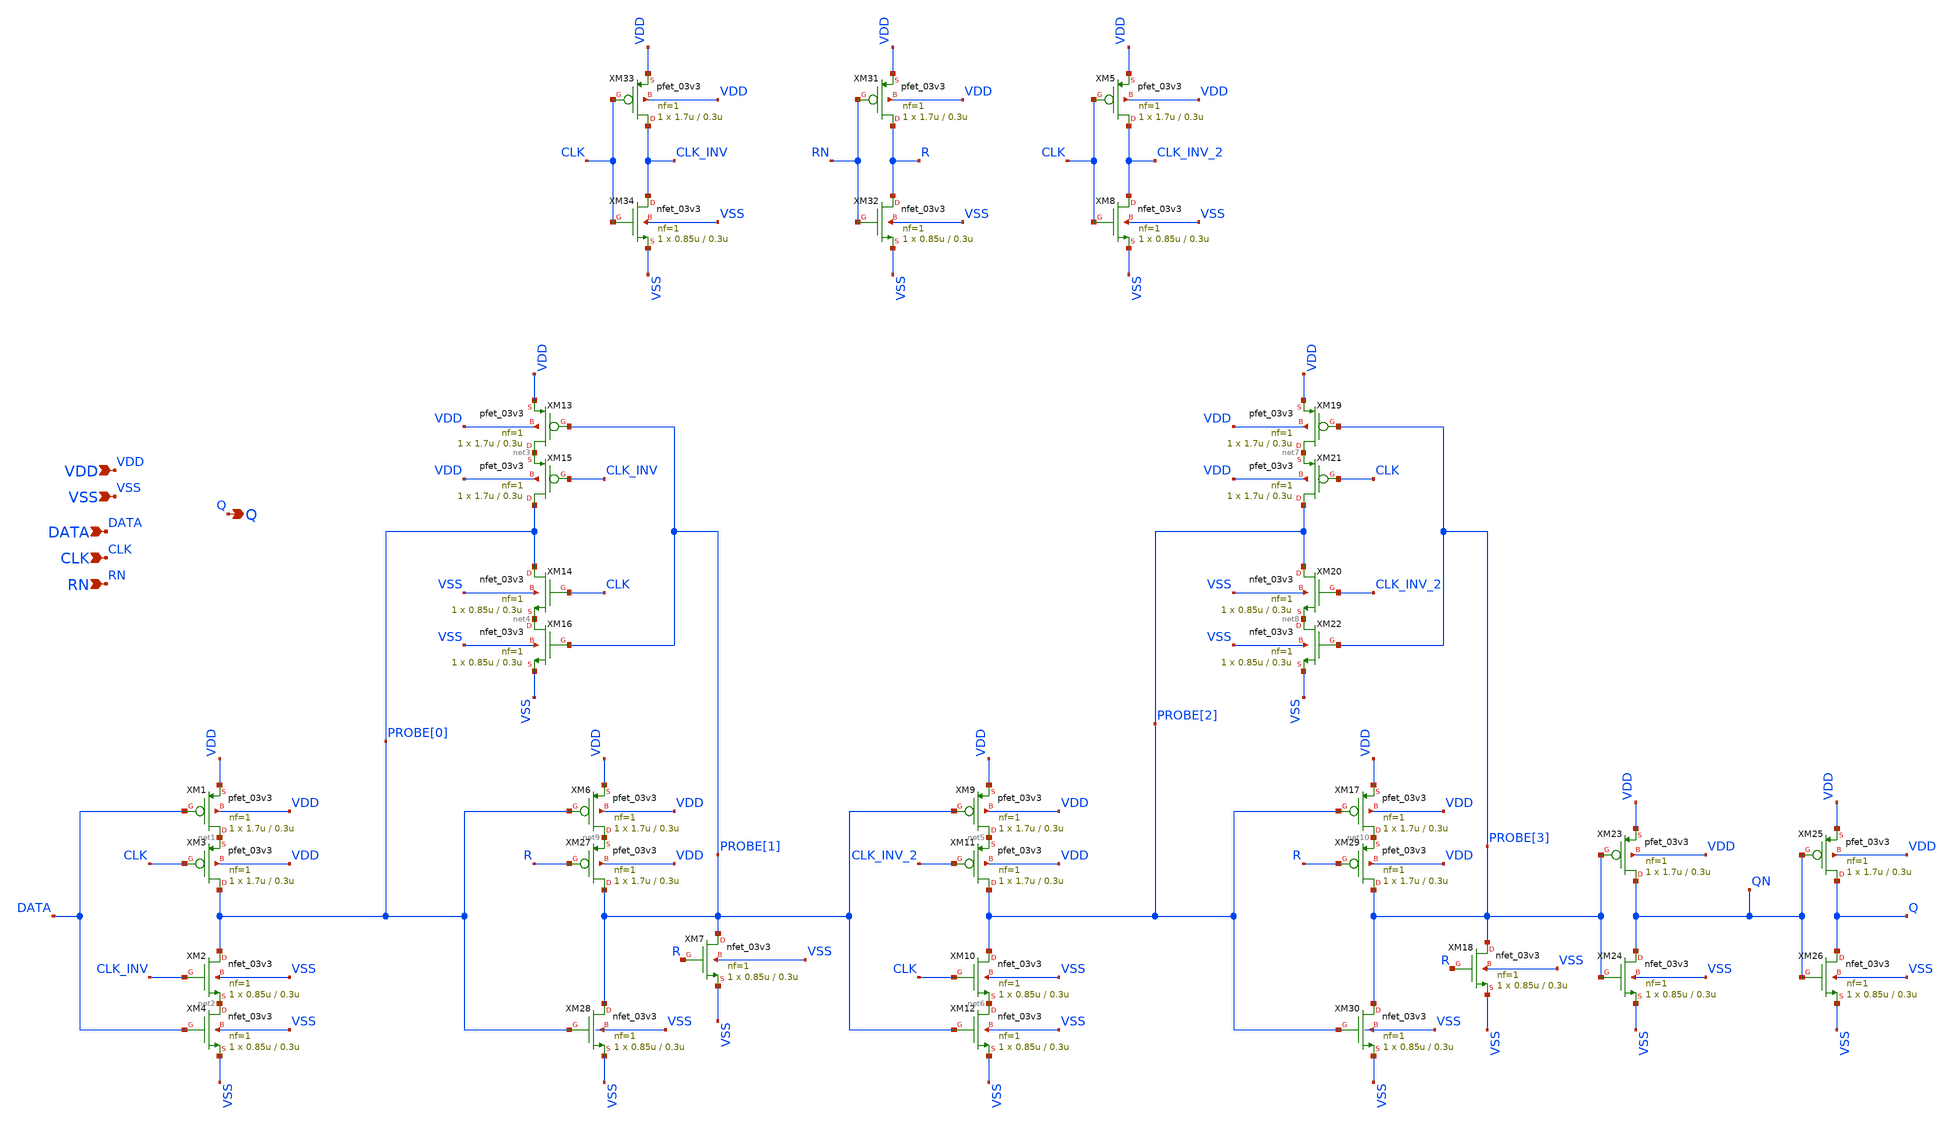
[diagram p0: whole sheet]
** sch_path: designs/cells/gf180mcu_voidwalkers_sc_sdffrnq_4/sch/d_flip_flop_r.sch
**.subckt d_flip_flop_r DATA VDD VSS Q CLK RN
*.ipin DATA
*.ipin VDD
*.ipin VSS
*.opin Q
*.ipin CLK
*.ipin RN
XM1 net1 DATA VDD VDD pfet_03v3 L=0.3u W=1.7u nf=1 ad='int((nf+1)/2) * W/nf * 0.18u' as='int((nf+2)/2) * W/nf * 0.18u'
+ pd='2*int((nf+1)/2) * (W/nf + 0.18u)' ps='2*int((nf+2)/2) * (W/nf + 0.18u)' nrd='0.18u / W' nrs='0.18u / W'
+ sa=0 sb=0 sd=0 m=1
XM2 PROBE[0] CLK_INV net2 VSS nfet_03v3 L=0.3u W=0.85u nf=1 ad='int((nf+1)/2) * W/nf * 0.18u' as='int((nf+2)/2) * W/nf * 0.18u'
+ pd='2*int((nf+1)/2) * (W/nf + 0.18u)' ps='2*int((nf+2)/2) * (W/nf + 0.18u)' nrd='0.18u / W' nrs='0.18u / W'
+ sa=0 sb=0 sd=0 m=1
XM3 PROBE[0] CLK net1 VDD pfet_03v3 L=0.3u W=1.7u nf=1 ad='int((nf+1)/2) * W/nf * 0.18u' as='int((nf+2)/2) * W/nf * 0.18u'
+ pd='2*int((nf+1)/2) * (W/nf + 0.18u)' ps='2*int((nf+2)/2) * (W/nf + 0.18u)' nrd='0.18u / W' nrs='0.18u / W'
+ sa=0 sb=0 sd=0 m=1
XM4 net2 DATA VSS VSS nfet_03v3 L=0.3u W=0.85u nf=1 ad='int((nf+1)/2) * W/nf * 0.18u' as='int((nf+2)/2) * W/nf * 0.18u'
+ pd='2*int((nf+1)/2) * (W/nf + 0.18u)' ps='2*int((nf+2)/2) * (W/nf + 0.18u)' nrd='0.18u / W' nrs='0.18u / W'
+ sa=0 sb=0 sd=0 m=1
XM5 CLK_INV_2 CLK VDD VDD pfet_03v3 L=0.3u W=1.7u nf=1 ad='int((nf+1)/2) * W/nf * 0.18u' as='int((nf+2)/2) * W/nf * 0.18u'
+ pd='2*int((nf+1)/2) * (W/nf + 0.18u)' ps='2*int((nf+2)/2) * (W/nf + 0.18u)' nrd='0.18u / W' nrs='0.18u / W'
+ sa=0 sb=0 sd=0 m=1
XM8 CLK_INV_2 CLK VSS VSS nfet_03v3 L=0.3u W=0.85u nf=1 ad='int((nf+1)/2) * W/nf * 0.18u' as='int((nf+2)/2) * W/nf * 0.18u'
+ pd='2*int((nf+1)/2) * (W/nf + 0.18u)' ps='2*int((nf+2)/2) * (W/nf + 0.18u)' nrd='0.18u / W' nrs='0.18u / W'
+ sa=0 sb=0 sd=0 m=1
XM13 net3 PROBE[1] VDD VDD pfet_03v3 L=0.3u W=1.7u nf=1 ad='int((nf+1)/2) * W/nf * 0.18u' as='int((nf+2)/2) * W/nf * 0.18u'
+ pd='2*int((nf+1)/2) * (W/nf + 0.18u)' ps='2*int((nf+2)/2) * (W/nf + 0.18u)' nrd='0.18u / W' nrs='0.18u / W'
+ sa=0 sb=0 sd=0 m=1
XM14 PROBE[0] CLK net4 VSS nfet_03v3 L=0.3u W=0.85u nf=1 ad='int((nf+1)/2) * W/nf * 0.18u' as='int((nf+2)/2) * W/nf * 0.18u'
+ pd='2*int((nf+1)/2) * (W/nf + 0.18u)' ps='2*int((nf+2)/2) * (W/nf + 0.18u)' nrd='0.18u / W' nrs='0.18u / W'
+ sa=0 sb=0 sd=0 m=1
XM15 PROBE[0] CLK_INV net3 VDD pfet_03v3 L=0.3u W=1.7u nf=1 ad='int((nf+1)/2) * W/nf * 0.18u' as='int((nf+2)/2) * W/nf * 0.18u'
+ pd='2*int((nf+1)/2) * (W/nf + 0.18u)' ps='2*int((nf+2)/2) * (W/nf + 0.18u)' nrd='0.18u / W' nrs='0.18u / W'
+ sa=0 sb=0 sd=0 m=1
XM16 net4 PROBE[1] VSS VSS nfet_03v3 L=0.3u W=0.85u nf=1 ad='int((nf+1)/2) * W/nf * 0.18u' as='int((nf+2)/2) * W/nf * 0.18u'
+ pd='2*int((nf+1)/2) * (W/nf + 0.18u)' ps='2*int((nf+2)/2) * (W/nf + 0.18u)' nrd='0.18u / W' nrs='0.18u / W'
+ sa=0 sb=0 sd=0 m=1
XM9 net5 PROBE[1] VDD VDD pfet_03v3 L=0.3u W=1.7u nf=1 ad='int((nf+1)/2) * W/nf * 0.18u' as='int((nf+2)/2) * W/nf * 0.18u'
+ pd='2*int((nf+1)/2) * (W/nf + 0.18u)' ps='2*int((nf+2)/2) * (W/nf + 0.18u)' nrd='0.18u / W' nrs='0.18u / W'
+ sa=0 sb=0 sd=0 m=1
XM10 PROBE[2] CLK net6 VSS nfet_03v3 L=0.3u W=0.85u nf=1 ad='int((nf+1)/2) * W/nf * 0.18u' as='int((nf+2)/2) * W/nf * 0.18u'
+ pd='2*int((nf+1)/2) * (W/nf + 0.18u)' ps='2*int((nf+2)/2) * (W/nf + 0.18u)' nrd='0.18u / W' nrs='0.18u / W'
+ sa=0 sb=0 sd=0 m=1
XM11 PROBE[2] CLK_INV_2 net5 VDD pfet_03v3 L=0.3u W=1.7u nf=1 ad='int((nf+1)/2) * W/nf * 0.18u' as='int((nf+2)/2) * W/nf * 0.18u'
+ pd='2*int((nf+1)/2) * (W/nf + 0.18u)' ps='2*int((nf+2)/2) * (W/nf + 0.18u)' nrd='0.18u / W' nrs='0.18u / W'
+ sa=0 sb=0 sd=0 m=1
XM12 net6 PROBE[1] VSS VSS nfet_03v3 L=0.3u W=0.85u nf=1 ad='int((nf+1)/2) * W/nf * 0.18u' as='int((nf+2)/2) * W/nf * 0.18u'
+ pd='2*int((nf+1)/2) * (W/nf + 0.18u)' ps='2*int((nf+2)/2) * (W/nf + 0.18u)' nrd='0.18u / W' nrs='0.18u / W'
+ sa=0 sb=0 sd=0 m=1
XM19 net7 PROBE[3] VDD VDD pfet_03v3 L=0.3u W=1.7u nf=1 ad='int((nf+1)/2) * W/nf * 0.18u' as='int((nf+2)/2) * W/nf * 0.18u'
+ pd='2*int((nf+1)/2) * (W/nf + 0.18u)' ps='2*int((nf+2)/2) * (W/nf + 0.18u)' nrd='0.18u / W' nrs='0.18u / W'
+ sa=0 sb=0 sd=0 m=1
XM20 PROBE[2] CLK_INV_2 net8 VSS nfet_03v3 L=0.3u W=0.85u nf=1 ad='int((nf+1)/2) * W/nf * 0.18u' as='int((nf+2)/2) * W/nf * 0.18u'
+ pd='2*int((nf+1)/2) * (W/nf + 0.18u)' ps='2*int((nf+2)/2) * (W/nf + 0.18u)' nrd='0.18u / W' nrs='0.18u / W'
+ sa=0 sb=0 sd=0 m=1
XM21 PROBE[2] CLK net7 VDD pfet_03v3 L=0.3u W=1.7u nf=1 ad='int((nf+1)/2) * W/nf * 0.18u' as='int((nf+2)/2) * W/nf * 0.18u'
+ pd='2*int((nf+1)/2) * (W/nf + 0.18u)' ps='2*int((nf+2)/2) * (W/nf + 0.18u)' nrd='0.18u / W' nrs='0.18u / W'
+ sa=0 sb=0 sd=0 m=1
XM22 net8 PROBE[3] VSS VSS nfet_03v3 L=0.3u W=0.85u nf=1 ad='int((nf+1)/2) * W/nf * 0.18u' as='int((nf+2)/2) * W/nf * 0.18u'
+ pd='2*int((nf+1)/2) * (W/nf + 0.18u)' ps='2*int((nf+2)/2) * (W/nf + 0.18u)' nrd='0.18u / W' nrs='0.18u / W'
+ sa=0 sb=0 sd=0 m=1
XM23 QN PROBE[3] VDD VDD pfet_03v3 L=0.3u W=1.7u nf=1 ad='int((nf+1)/2) * W/nf * 0.18u' as='int((nf+2)/2) * W/nf * 0.18u'
+ pd='2*int((nf+1)/2) * (W/nf + 0.18u)' ps='2*int((nf+2)/2) * (W/nf + 0.18u)' nrd='0.18u / W' nrs='0.18u / W'
+ sa=0 sb=0 sd=0 m=1
XM24 QN PROBE[3] VSS VSS nfet_03v3 L=0.3u W=0.85u nf=1 ad='int((nf+1)/2) * W/nf * 0.18u' as='int((nf+2)/2) * W/nf * 0.18u'
+ pd='2*int((nf+1)/2) * (W/nf + 0.18u)' ps='2*int((nf+2)/2) * (W/nf + 0.18u)' nrd='0.18u / W' nrs='0.18u / W'
+ sa=0 sb=0 sd=0 m=1
XM25 Q QN VDD VDD pfet_03v3 L=0.3u W=1.7u nf=1 ad='int((nf+1)/2) * W/nf * 0.18u' as='int((nf+2)/2) * W/nf * 0.18u'
+ pd='2*int((nf+1)/2) * (W/nf + 0.18u)' ps='2*int((nf+2)/2) * (W/nf + 0.18u)' nrd='0.18u / W' nrs='0.18u / W'
+ sa=0 sb=0 sd=0 m=1
XM26 Q QN VSS VSS nfet_03v3 L=0.3u W=0.85u nf=1 ad='int((nf+1)/2) * W/nf * 0.18u' as='int((nf+2)/2) * W/nf * 0.18u'
+ pd='2*int((nf+1)/2) * (W/nf + 0.18u)' ps='2*int((nf+2)/2) * (W/nf + 0.18u)' nrd='0.18u / W' nrs='0.18u / W'
+ sa=0 sb=0 sd=0 m=1
XM6 net9 PROBE[0] VDD VDD pfet_03v3 L=0.3u W=1.7u nf=1 ad='int((nf+1)/2) * W/nf * 0.18u' as='int((nf+2)/2) * W/nf * 0.18u'
+ pd='2*int((nf+1)/2) * (W/nf + 0.18u)' ps='2*int((nf+2)/2) * (W/nf + 0.18u)' nrd='0.18u / W' nrs='0.18u / W'
+ sa=0 sb=0 sd=0 m=1
XM27 PROBE[1] R net9 VDD pfet_03v3 L=0.3u W=1.7u nf=1 ad='int((nf+1)/2) * W/nf * 0.18u' as='int((nf+2)/2) * W/nf * 0.18u'
+ pd='2*int((nf+1)/2) * (W/nf + 0.18u)' ps='2*int((nf+2)/2) * (W/nf + 0.18u)' nrd='0.18u / W' nrs='0.18u / W'
+ sa=0 sb=0 sd=0 m=1
XM28 PROBE[1] PROBE[0] VSS VSS nfet_03v3 L=0.3u W=0.85u nf=1 ad='int((nf+1)/2) * W/nf * 0.18u' as='int((nf+2)/2) * W/nf * 0.18u'
+ pd='2*int((nf+1)/2) * (W/nf + 0.18u)' ps='2*int((nf+2)/2) * (W/nf + 0.18u)' nrd='0.18u / W' nrs='0.18u / W'
+ sa=0 sb=0 sd=0 m=1
XM17 net10 PROBE[2] VDD VDD pfet_03v3 L=0.3u W=1.7u nf=1 ad='int((nf+1)/2) * W/nf * 0.18u' as='int((nf+2)/2) * W/nf * 0.18u'
+ pd='2*int((nf+1)/2) * (W/nf + 0.18u)' ps='2*int((nf+2)/2) * (W/nf + 0.18u)' nrd='0.18u / W' nrs='0.18u / W'
+ sa=0 sb=0 sd=0 m=1
XM29 PROBE[3] R net10 VDD pfet_03v3 L=0.3u W=1.7u nf=1 ad='int((nf+1)/2) * W/nf * 0.18u' as='int((nf+2)/2) * W/nf * 0.18u'
+ pd='2*int((nf+1)/2) * (W/nf + 0.18u)' ps='2*int((nf+2)/2) * (W/nf + 0.18u)' nrd='0.18u / W' nrs='0.18u / W'
+ sa=0 sb=0 sd=0 m=1
XM30 PROBE[3] PROBE[2] VSS VSS nfet_03v3 L=0.3u W=0.85u nf=1 ad='int((nf+1)/2) * W/nf * 0.18u' as='int((nf+2)/2) * W/nf * 0.18u'
+ pd='2*int((nf+1)/2) * (W/nf + 0.18u)' ps='2*int((nf+2)/2) * (W/nf + 0.18u)' nrd='0.18u / W' nrs='0.18u / W'
+ sa=0 sb=0 sd=0 m=1
XM7 PROBE[1] R VSS VSS nfet_03v3 L=0.3u W=0.85u nf=1 ad='int((nf+1)/2) * W/nf * 0.18u' as='int((nf+2)/2) * W/nf * 0.18u'
+ pd='2*int((nf+1)/2) * (W/nf + 0.18u)' ps='2*int((nf+2)/2) * (W/nf + 0.18u)' nrd='0.18u / W' nrs='0.18u / W'
+ sa=0 sb=0 sd=0 m=1
XM18 PROBE[3] R VSS VSS nfet_03v3 L=0.3u W=0.85u nf=1 ad='int((nf+1)/2) * W/nf * 0.18u' as='int((nf+2)/2) * W/nf * 0.18u'
+ pd='2*int((nf+1)/2) * (W/nf + 0.18u)' ps='2*int((nf+2)/2) * (W/nf + 0.18u)' nrd='0.18u / W' nrs='0.18u / W'
+ sa=0 sb=0 sd=0 m=1
XM31 R RN VDD VDD pfet_03v3 L=0.3u W=1.7u nf=1 ad='int((nf+1)/2) * W/nf * 0.18u' as='int((nf+2)/2) * W/nf * 0.18u'
+ pd='2*int((nf+1)/2) * (W/nf + 0.18u)' ps='2*int((nf+2)/2) * (W/nf + 0.18u)' nrd='0.18u / W' nrs='0.18u / W'
+ sa=0 sb=0 sd=0 m=1
XM32 R RN VSS VSS nfet_03v3 L=0.3u W=0.85u nf=1 ad='int((nf+1)/2) * W/nf * 0.18u' as='int((nf+2)/2) * W/nf * 0.18u'
+ pd='2*int((nf+1)/2) * (W/nf + 0.18u)' ps='2*int((nf+2)/2) * (W/nf + 0.18u)' nrd='0.18u / W' nrs='0.18u / W'
+ sa=0 sb=0 sd=0 m=1
XM33 CLK_INV CLK VDD VDD pfet_03v3 L=0.3u W=1.7u nf=1 ad='int((nf+1)/2) * W/nf * 0.18u' as='int((nf+2)/2) * W/nf * 0.18u'
+ pd='2*int((nf+1)/2) * (W/nf + 0.18u)' ps='2*int((nf+2)/2) * (W/nf + 0.18u)' nrd='0.18u / W' nrs='0.18u / W'
+ sa=0 sb=0 sd=0 m=1
XM34 CLK_INV CLK VSS VSS nfet_03v3 L=0.3u W=0.85u nf=1 ad='int((nf+1)/2) * W/nf * 0.18u' as='int((nf+2)/2) * W/nf * 0.18u'
+ pd='2*int((nf+1)/2) * (W/nf + 0.18u)' ps='2*int((nf+2)/2) * (W/nf + 0.18u)' nrd='0.18u / W' nrs='0.18u / W'
+ sa=0 sb=0 sd=0 m=1
**.ends
.end
